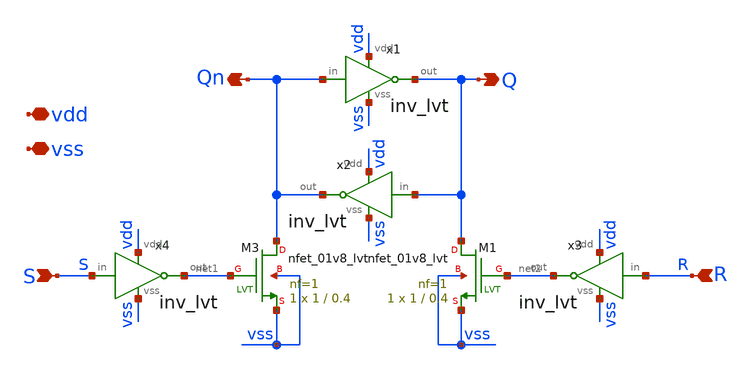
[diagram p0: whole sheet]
** sch_path: xschem/sar_10b/latch/latch.sch
**.subckt latch S R vss vdd Q Qn
*.ipin S
*.ipin R
*.iopin vss
*.iopin vdd
*.opin Q
*.opin Qn
x1 vdd Qn Q vss inv_lvt
x2 vdd Q Qn vss inv_lvt
x3 vdd R net2 vss inv_lvt
x4 vdd S net1 vss inv_lvt
XM3 Qn net1 vss vss sky130_fd_pr__nfet_01v8_lvt L=0.4 W=1 nf=1 ad='int((nf+1)/2) * W/nf * 0.29' as='int((nf+2)/2) * W/nf * 0.29'
+ pd='2*int((nf+1)/2) * (W/nf + 0.29)' ps='2*int((nf+2)/2) * (W/nf + 0.29)' nrd='0.29 / W' nrs='0.29 / W'
+ sa=0 sb=0 sd=0 mult=1 m=1
XM1 Q net2 vss vss sky130_fd_pr__nfet_01v8_lvt L=0.4 W=1 nf=1 ad='int((nf+1)/2) * W/nf * 0.29' as='int((nf+2)/2) * W/nf * 0.29'
+ pd='2*int((nf+1)/2) * (W/nf + 0.29)' ps='2*int((nf+2)/2) * (W/nf + 0.29)' nrd='0.29 / W' nrs='0.29 / W'
+ sa=0 sb=0 sd=0 mult=1 m=1
**.ends

* expanding   symbol:  logic/inv_lvt.sym # of pins=4
** sym_path: xschem/logic/inv_lvt.sym
** sch_path: xschem/logic/inv_lvt.sch
.subckt inv_lvt vdd in out vss
*.iopin vdd
*.iopin vss
*.ipin in
*.opin out
XM1 out in vss vss sky130_fd_pr__nfet_01v8_lvt L=0.4 W=1 nf=1 ad='int((nf+1)/2) * W/nf * 0.29' as='int((nf+2)/2) * W/nf * 0.29'
+ pd='2*int((nf+1)/2) * (W/nf + 0.29)' ps='2*int((nf+2)/2) * (W/nf + 0.29)' nrd='0.29 / W' nrs='0.29 / W'
+ sa=0 sb=0 sd=0 mult=1 m=1
XM2 out in vdd vdd sky130_fd_pr__pfet_01v8_lvt L=0.4 W=1 nf=1 ad='int((nf+1)/2) * W/nf * 0.29' as='int((nf+2)/2) * W/nf * 0.29'
+ pd='2*int((nf+1)/2) * (W/nf + 0.29)' ps='2*int((nf+2)/2) * (W/nf + 0.29)' nrd='0.29 / W' nrs='0.29 / W'
+ sa=0 sb=0 sd=0 mult=1 m=1
.ends

.end
